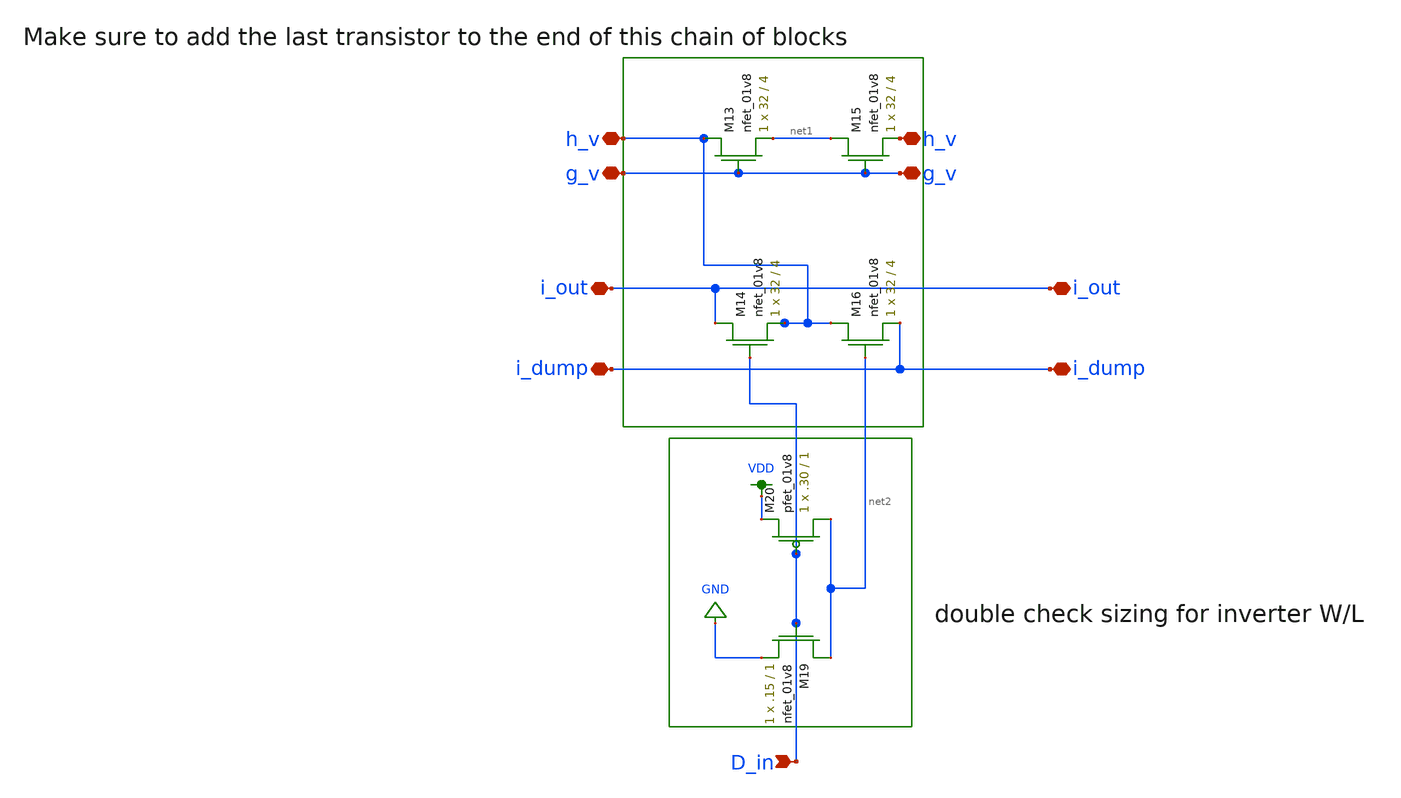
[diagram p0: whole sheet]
** sch_path: schemas/LDS_DAC_block.sch
**.subckt LDS_DAC_block g_v h_v g_v i_out i_dump h_v D_in i_out i_dump
*.iopin g_v
*.iopin h_v
*.iopin g_v
*.iopin i_out
*.iopin i_dump
*.iopin h_v
*.ipin D_in
*.iopin i_out
*.iopin i_dump
XM13 h_v g_v net1 GND sky130_fd_pr__nfet_01v8 L=4 W=32 nf=1 ad='int((nf+1)/2) * W/nf * 0.29' as='int((nf+2)/2) * W/nf * 0.29'
+ pd='2*int((nf+1)/2) * (W/nf + 0.29)' ps='2*int((nf+2)/2) * (W/nf + 0.29)' nrd='0.29 / W' nrs='0.29 / W'
+ sa=0 sb=0 sd=0 mult=1 m=1
XM14 i_out D_in h_v GND sky130_fd_pr__nfet_01v8 L=4 W=32 nf=1 ad='int((nf+1)/2) * W/nf * 0.29' as='int((nf+2)/2) * W/nf * 0.29'
+ pd='2*int((nf+1)/2) * (W/nf + 0.29)' ps='2*int((nf+2)/2) * (W/nf + 0.29)' nrd='0.29 / W' nrs='0.29 / W'
+ sa=0 sb=0 sd=0 mult=1 m=1
XM15 net1 g_v h_v GND sky130_fd_pr__nfet_01v8 L=4 W=32 nf=1 ad='int((nf+1)/2) * W/nf * 0.29' as='int((nf+2)/2) * W/nf * 0.29'
+ pd='2*int((nf+1)/2) * (W/nf + 0.29)' ps='2*int((nf+2)/2) * (W/nf + 0.29)' nrd='0.29 / W' nrs='0.29 / W'
+ sa=0 sb=0 sd=0 mult=1 m=1
XM16 h_v net2 i_dump GND sky130_fd_pr__nfet_01v8 L=4 W=32 nf=1 ad='int((nf+1)/2) * W/nf * 0.29' as='int((nf+2)/2) * W/nf * 0.29'
+ pd='2*int((nf+1)/2) * (W/nf + 0.29)' ps='2*int((nf+2)/2) * (W/nf + 0.29)' nrd='0.29 / W' nrs='0.29 / W'
+ sa=0 sb=0 sd=0 mult=1 m=1
XM19 net2 D_in GND GND sky130_fd_pr__nfet_01v8 L=1 W=.15 nf=1 ad='int((nf+1)/2) * W/nf * 0.29' as='int((nf+2)/2) * W/nf * 0.29'
+ pd='2*int((nf+1)/2) * (W/nf + 0.29)' ps='2*int((nf+2)/2) * (W/nf + 0.29)' nrd='0.29 / W' nrs='0.29 / W'
+ sa=0 sb=0 sd=0 mult=1 m=1
XM20 net2 D_in VDD VDD sky130_fd_pr__pfet_01v8 L=1 W=.30 nf=1 ad='int((nf+1)/2) * W/nf * 0.29' as='int((nf+2)/2) * W/nf * 0.29'
+ pd='2*int((nf+1)/2) * (W/nf + 0.29)' ps='2*int((nf+2)/2) * (W/nf + 0.29)' nrd='0.29 / W' nrs='0.29 / W'
+ sa=0 sb=0 sd=0 mult=1 m=1
**.ends
.GLOBAL VDD
.GLOBAL GND
.end
